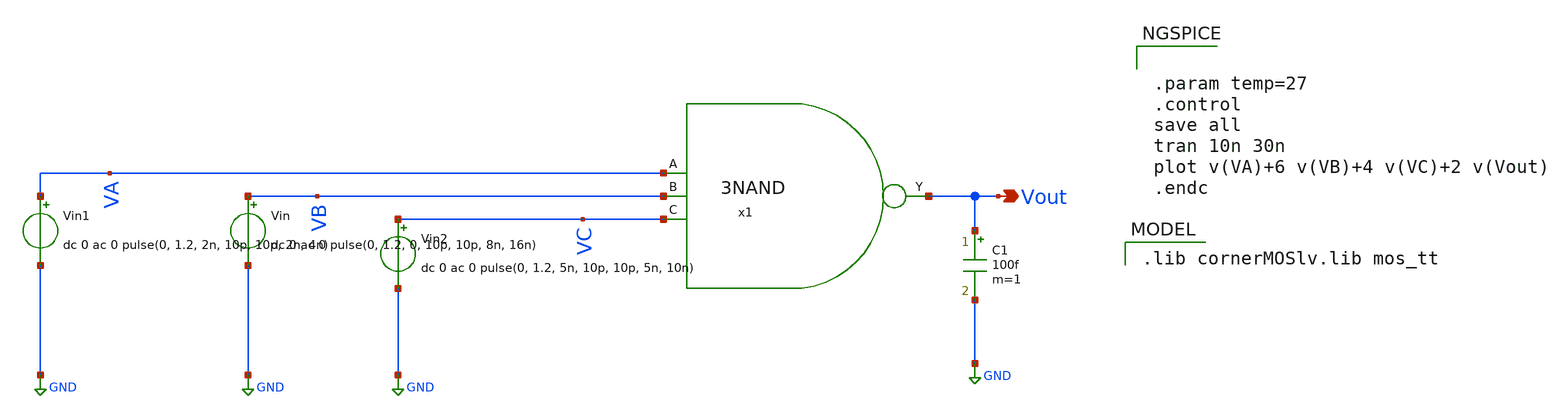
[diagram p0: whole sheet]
** sch_path: Team Designs/Team 1 Design/design_data/xschem/3_Input_NAND/3NAND_tb.sch
**.subckt 3NAND_tb Vout
*.opin Vout
Vin VB GND dc 0 ac 0 pulse(0, 1.2, 0, 10p, 10p, 8n, 16n)
Vin1 VA GND dc 0 ac 0 pulse(0, 1.2, 2n, 10p, 10p, 2n, 4n)
C1 Vout GND 100f m=1
Vin2 VC GND dc 0 ac 0 pulse(0, 1.2, 5n, 10p, 10p, 5n, 10n)
x1 Vout VA VB VC 3NAND
**** begin user architecture code
 .lib cornerMOSlv.lib mos_tt



.param temp=27
.control
save all
tran 10n 30n
plot v(VA)+6 v(VB)+4 v(VC)+2 v(Vout)
.endc


**** end user architecture code
**.ends

* expanding   symbol:  /foss/designs/Team1/3NAND/3NAND.sym # of pins=4
** sym_path: Team 1 Design/design_data/xschem/3_Input_NAND/3NAND.sym
** sch_path: Team 1 Design/design_data/xschem/3_Input_NAND/3NAND.sch
.subckt 3NAND Y A B C
*.ipin A
*.ipin B
*.ipin C
*.opin Y
XM1 Y A Vdd Vdd sg13_lv_pmos w=2u l=0.13u ng=1 m=1 mm_ok=1
XM2 Y B Vdd Vdd sg13_lv_pmos w=2u l=0.13u ng=1 m=1 mm_ok=1
XM3 Y C Vdd Vdd sg13_lv_pmos w=2u l=0.13u ng=1 m=1 mm_ok=1
XM4 Y A net1 GND sg13_lv_nmos w=1u l=0.13u ng=1 m=1 mm_ok=1
XM5 net1 B net2 GND sg13_lv_nmos w=1u l=0.13u ng=1 m=1 mm_ok=1
XM6 net2 C GND GND sg13_lv_nmos w=1u l=0.13u ng=1 m=1 mm_ok=1
V1 Vdd GND 1.2
.ends

.GLOBAL GND
.end
